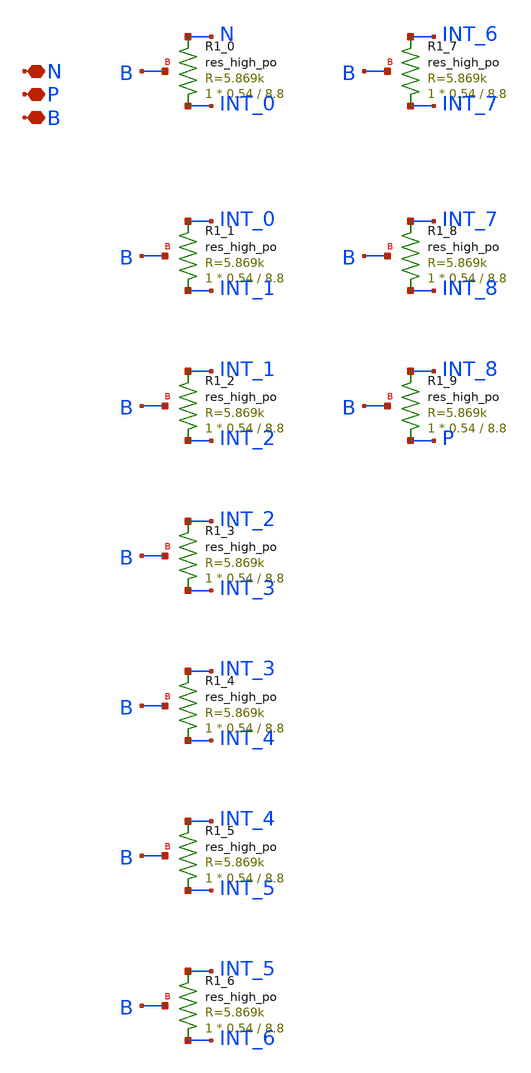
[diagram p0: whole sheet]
** sch_path: ip/sun_tr_sky130nm/design/SUN_TR_SKY130NM/SUNTR_RES100.sch
**.subckt SUNTR_RES100 N P B
*.iopin N
*.iopin P
*.iopin B
XR1_0 INT_0 N B sky130_fd_pr__res_high_po W=0.54 L=8.8 mult=1 m=1
XR1_1 INT_1 INT_0 B sky130_fd_pr__res_high_po W=0.54 L=8.8 mult=1 m=1
XR1_2 INT_2 INT_1 B sky130_fd_pr__res_high_po W=0.54 L=8.8 mult=1 m=1
XR1_3 INT_3 INT_2 B sky130_fd_pr__res_high_po W=0.54 L=8.8 mult=1 m=1
XR1_4 INT_4 INT_3 B sky130_fd_pr__res_high_po W=0.54 L=8.8 mult=1 m=1
XR1_5 INT_5 INT_4 B sky130_fd_pr__res_high_po W=0.54 L=8.8 mult=1 m=1
XR1_6 INT_6 INT_5 B sky130_fd_pr__res_high_po W=0.54 L=8.8 mult=1 m=1
XR1_7 INT_7 INT_6 B sky130_fd_pr__res_high_po W=0.54 L=8.8 mult=1 m=1
XR1_8 INT_8 INT_7 B sky130_fd_pr__res_high_po W=0.54 L=8.8 mult=1 m=1
XR1_9 P INT_8 B sky130_fd_pr__res_high_po W=0.54 L=8.8 mult=1 m=1
**.ends
.end
